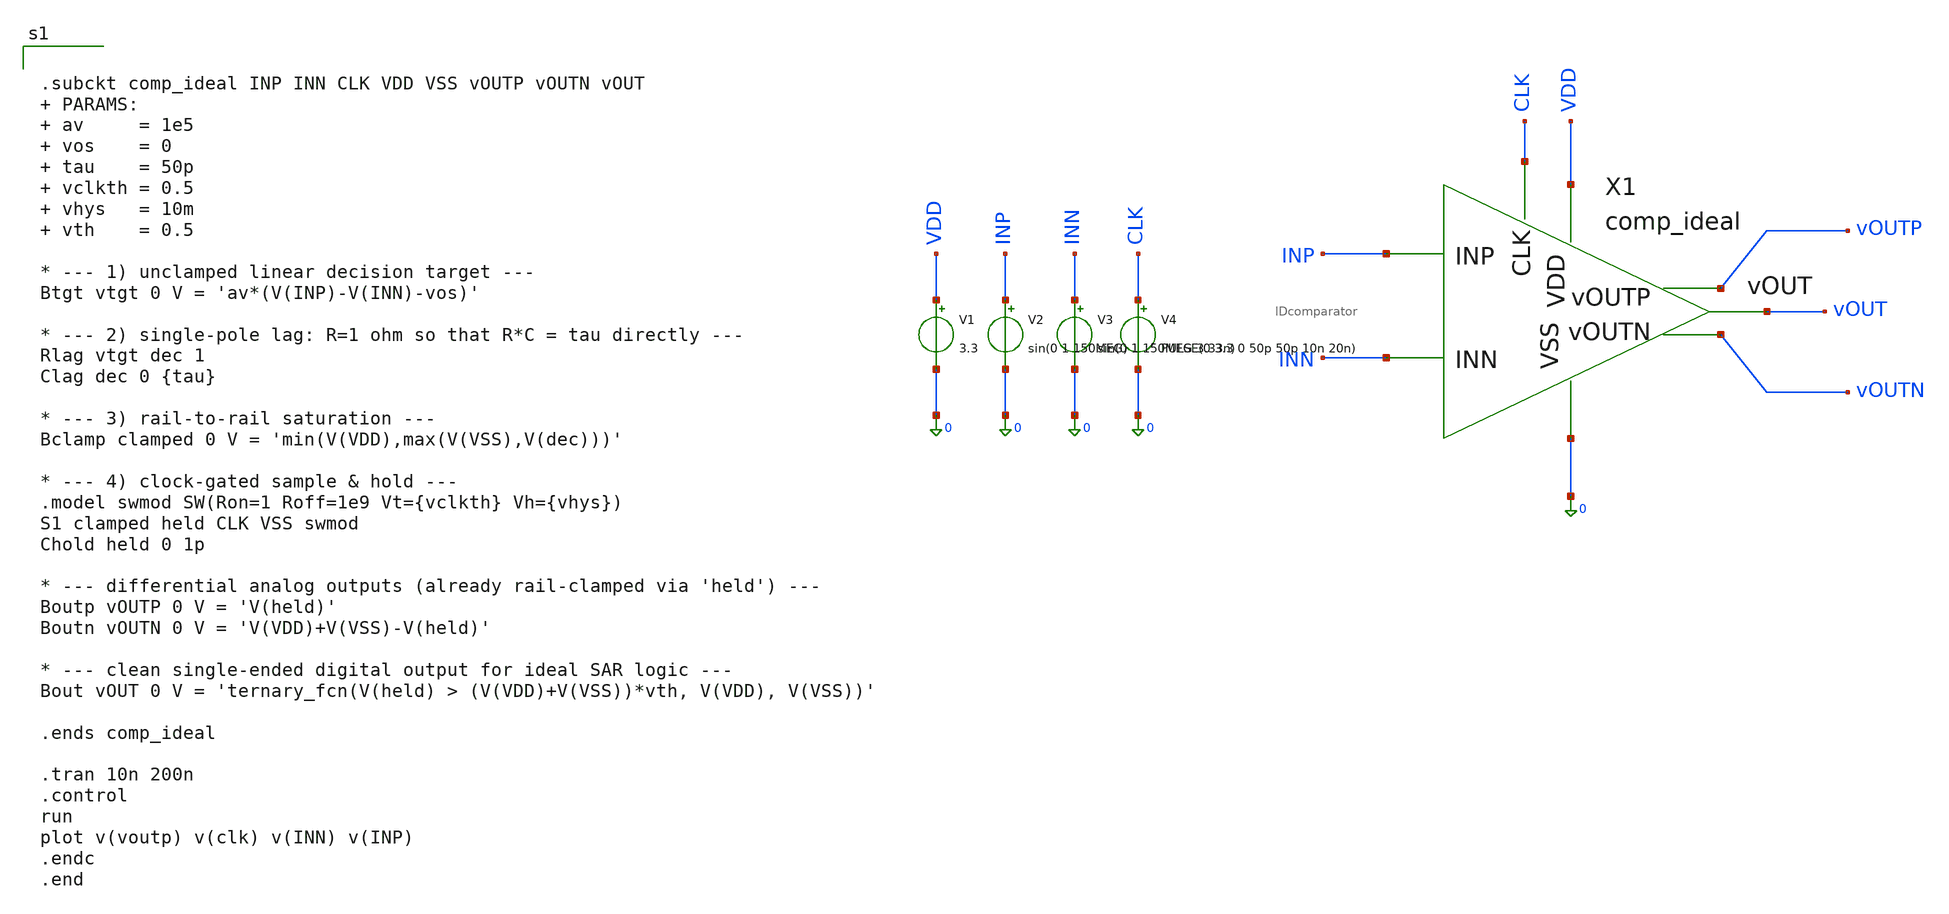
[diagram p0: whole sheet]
** sch_path: analog/IDcomparator/sim/IDcomptest.sch
**.subckt IDcomptest
V1 VDD 0 3.3
V2 INP 0 sin(0 1 150MEG)
V3 INN 0 sin(0 1 150MEG 3.33n)
V4 CLK 0 PULSE(0 3.3 0 50p 50p 10n 20n)
X1 INP INN CLK VDD 0 vOUTP vOUTN vOUT comp_ideal
**** begin user architecture code


.subckt comp_ideal INP INN CLK VDD VSS vOUTP vOUTN vOUT  PARAMS:  av     = 1e5  vos    = 0  tau    =
+ 50p  vclkth = 0.5  vhys   = 10m  vth    = 0.5

* --- 1) unclamped linear decision target ---
Btgt vtgt 0 V = 'av*(V(INP)-V(INN)-vos)'

* --- 2) single-pole lag: R=1 ohm so that R*C = tau directly ---
Rlag vtgt dec 1
Clag dec 0 {tau}

* --- 3) rail-to-rail saturation ---
Bclamp clamped 0 V = 'min(V(VDD),max(V(VSS),V(dec)))'

* --- 4) clock-gated sample & hold ---
.model swmod SW(Ron=1 Roff=1e9 Vt={vclkth} Vh={vhys})
S1 clamped held CLK VSS swmod
Chold held 0 1p

* --- differential analog outputs (already rail-clamped via 'held') ---
Boutp vOUTP 0 V = 'V(held)'
Boutn vOUTN 0 V = 'V(VDD)+V(VSS)-V(held)'

* --- clean single-ended digital output for ideal SAR logic ---
Bout vOUT 0 V = 'ternary_fcn(V(held) > (V(VDD)+V(VSS))*vth, V(VDD), V(VSS))'

.ends comp_ideal

.tran 10n 200n
.control
run
plot v(voutp) v(clk) v(INN) v(INP)
.endc
.end


**** end user architecture code
**.ends
.end
